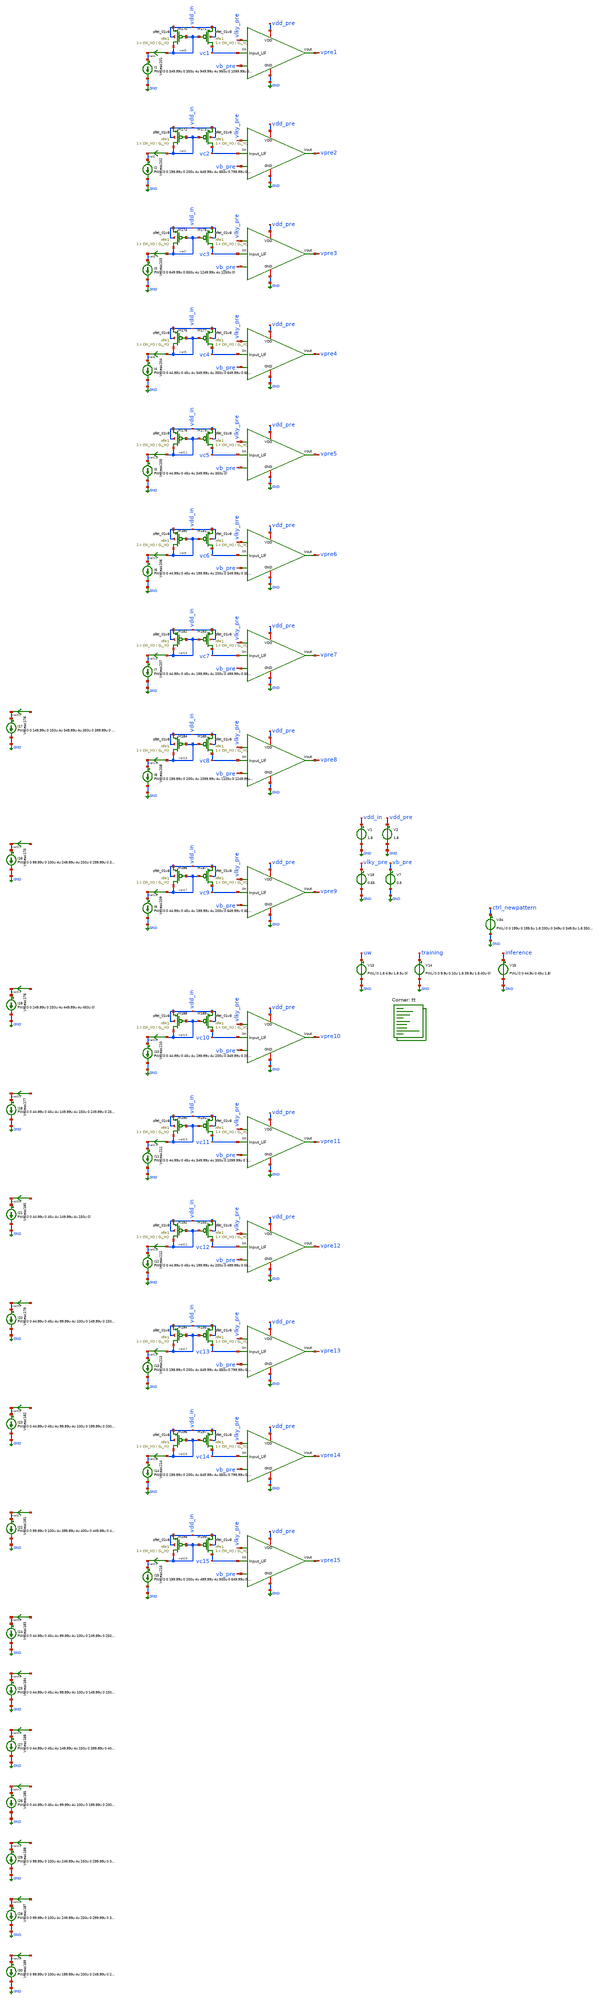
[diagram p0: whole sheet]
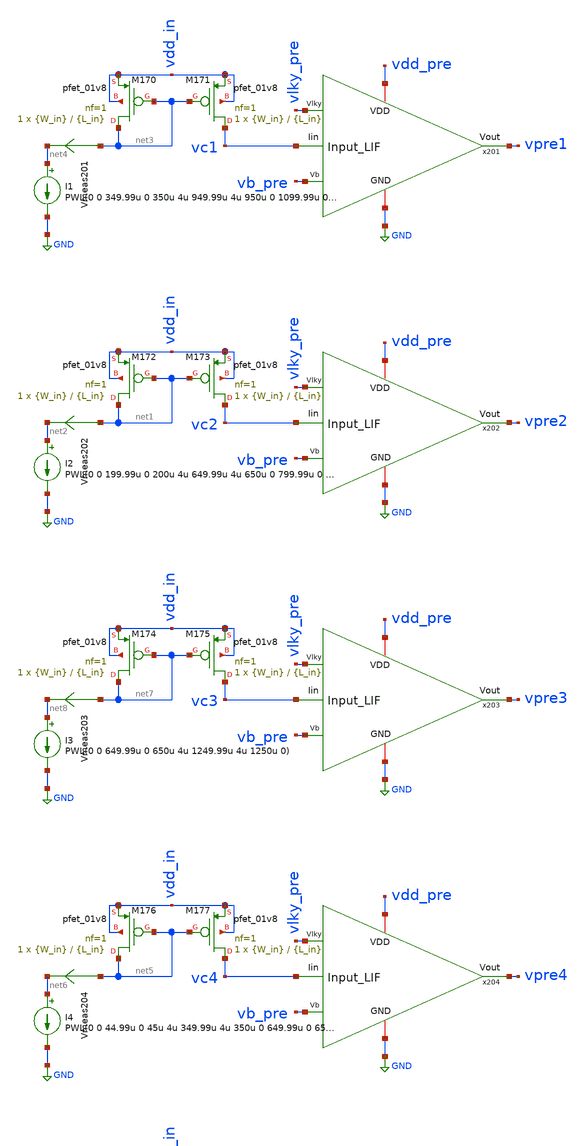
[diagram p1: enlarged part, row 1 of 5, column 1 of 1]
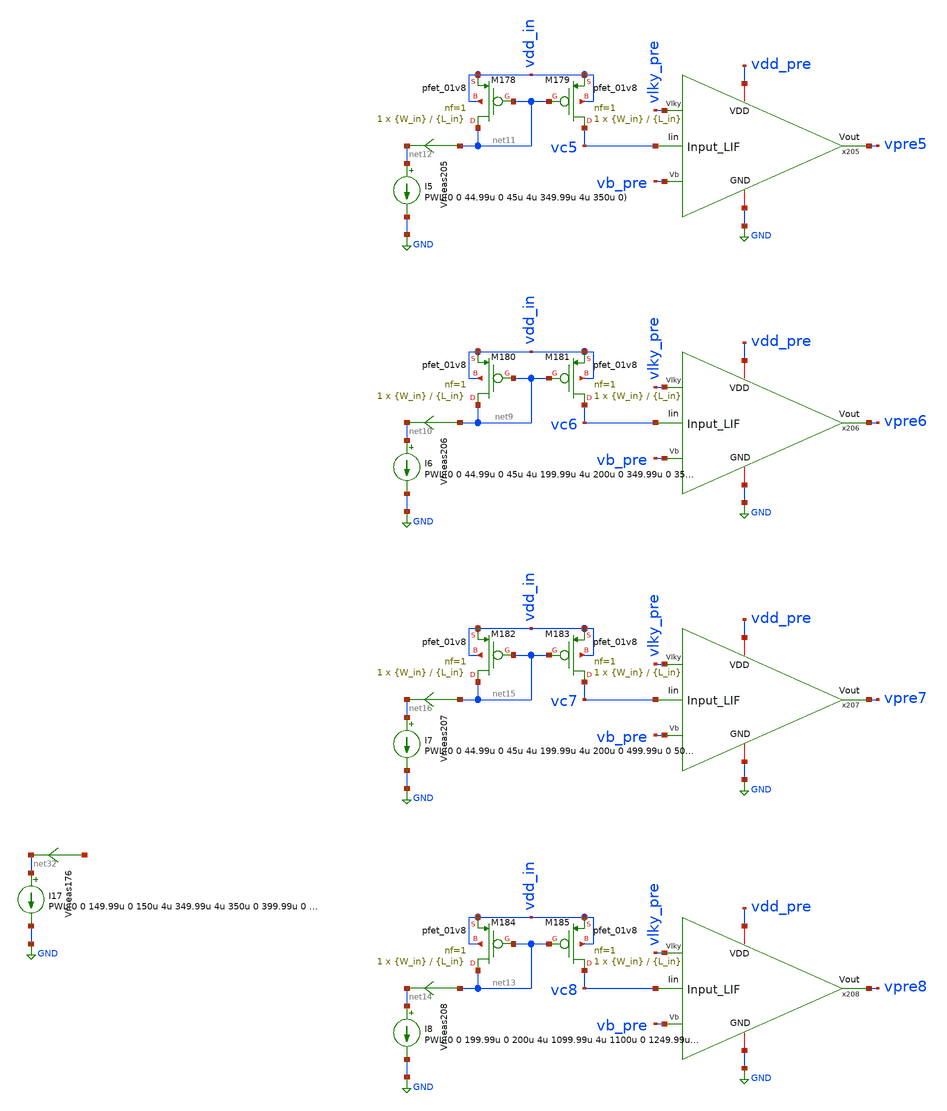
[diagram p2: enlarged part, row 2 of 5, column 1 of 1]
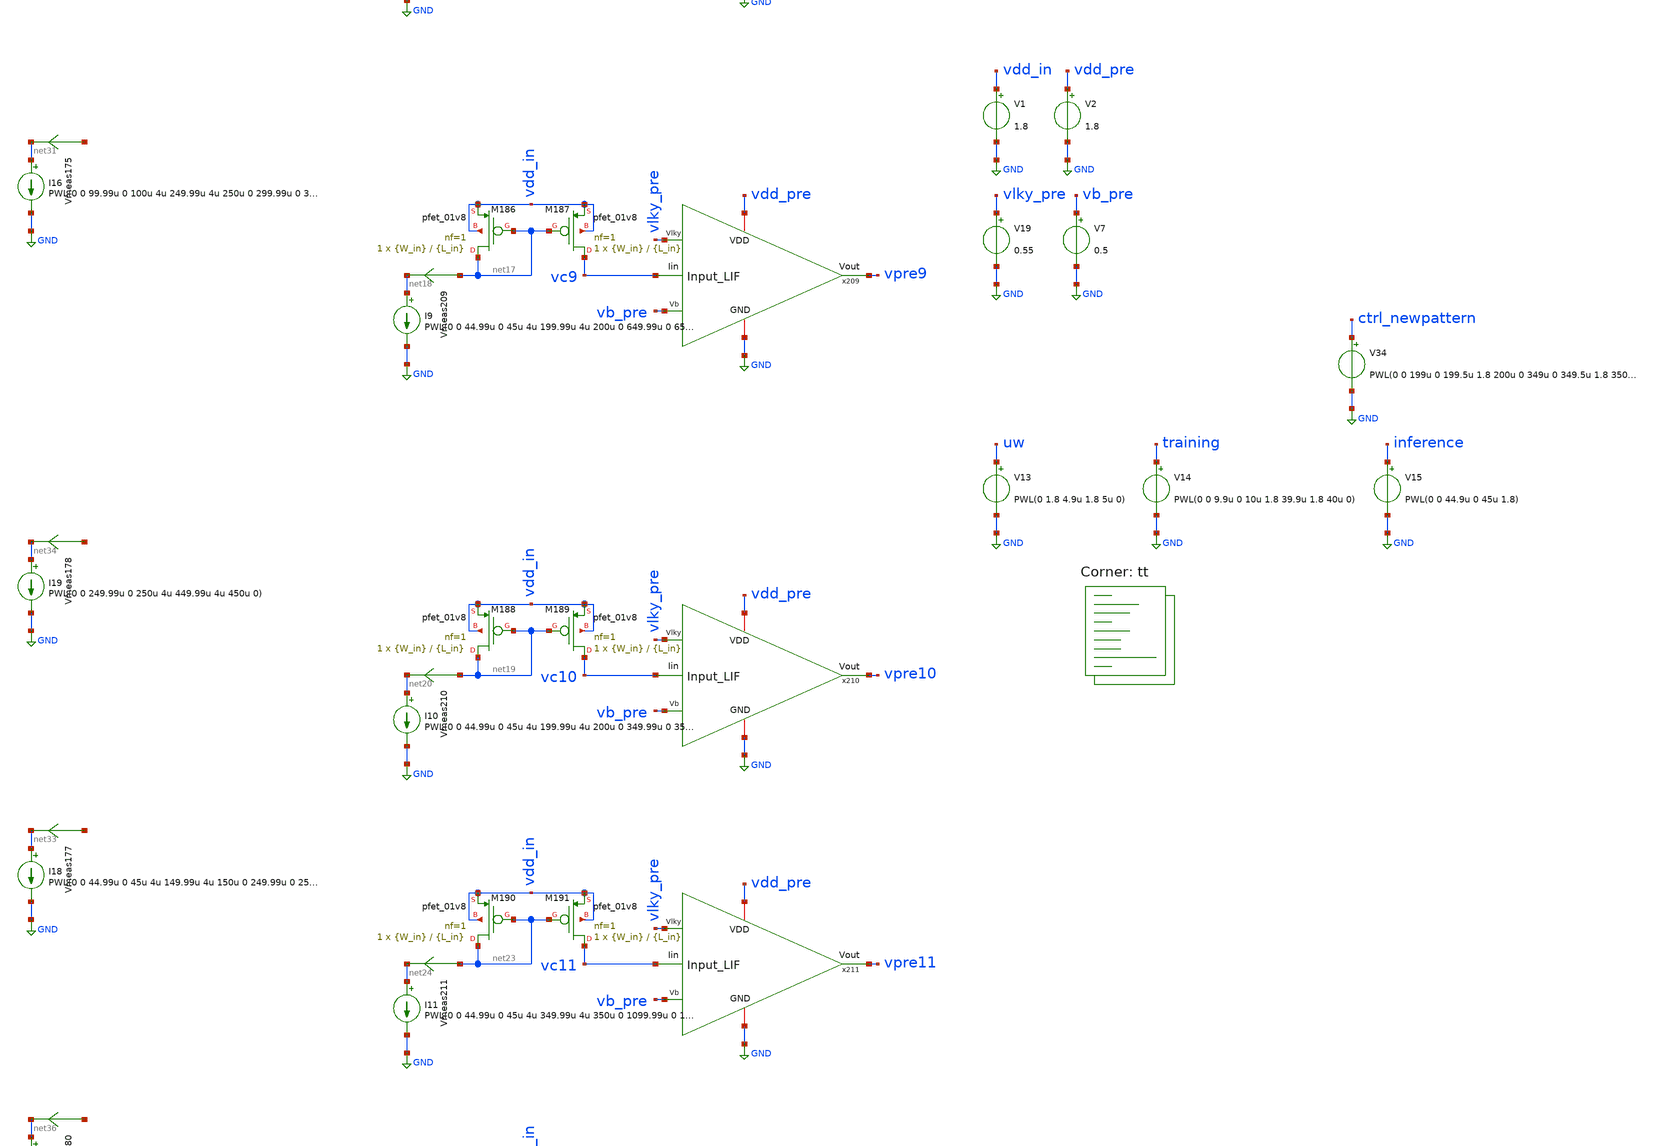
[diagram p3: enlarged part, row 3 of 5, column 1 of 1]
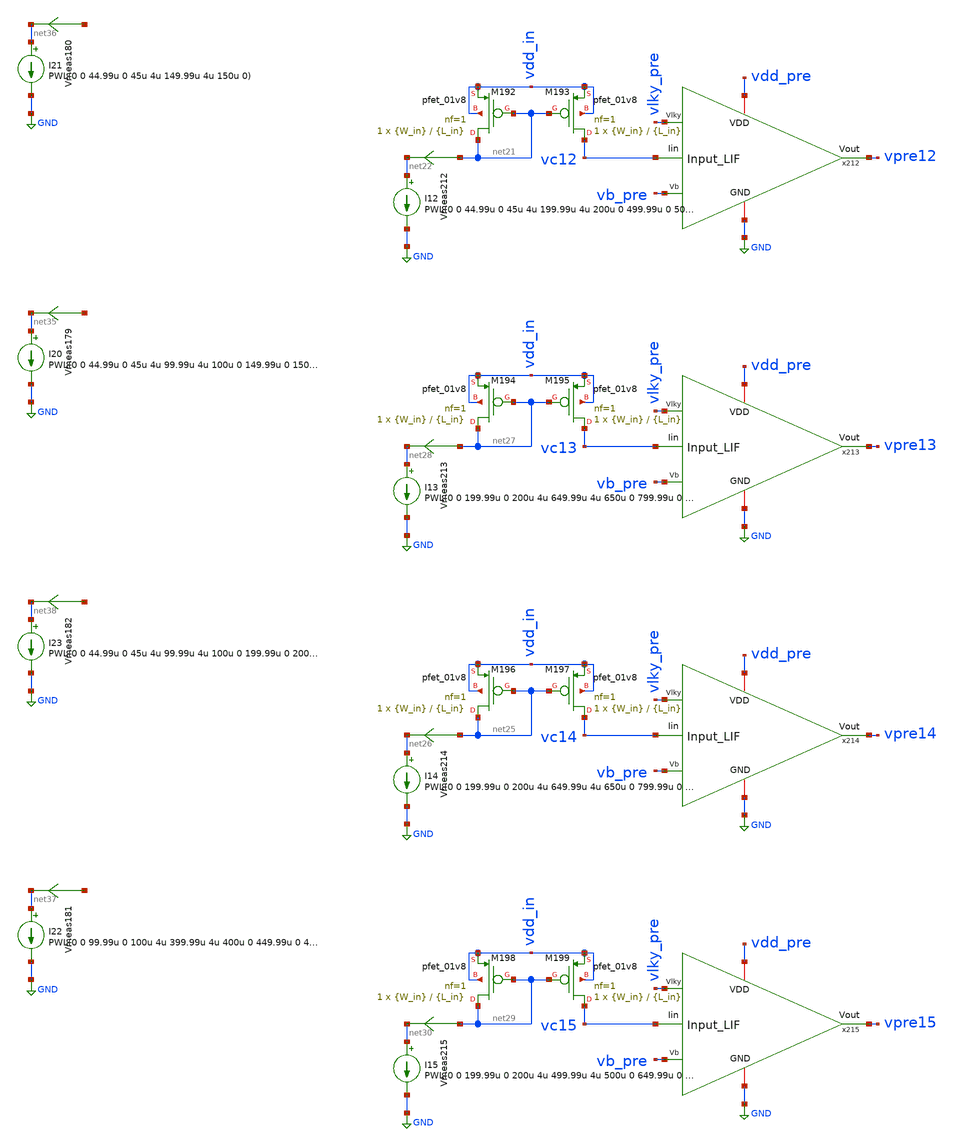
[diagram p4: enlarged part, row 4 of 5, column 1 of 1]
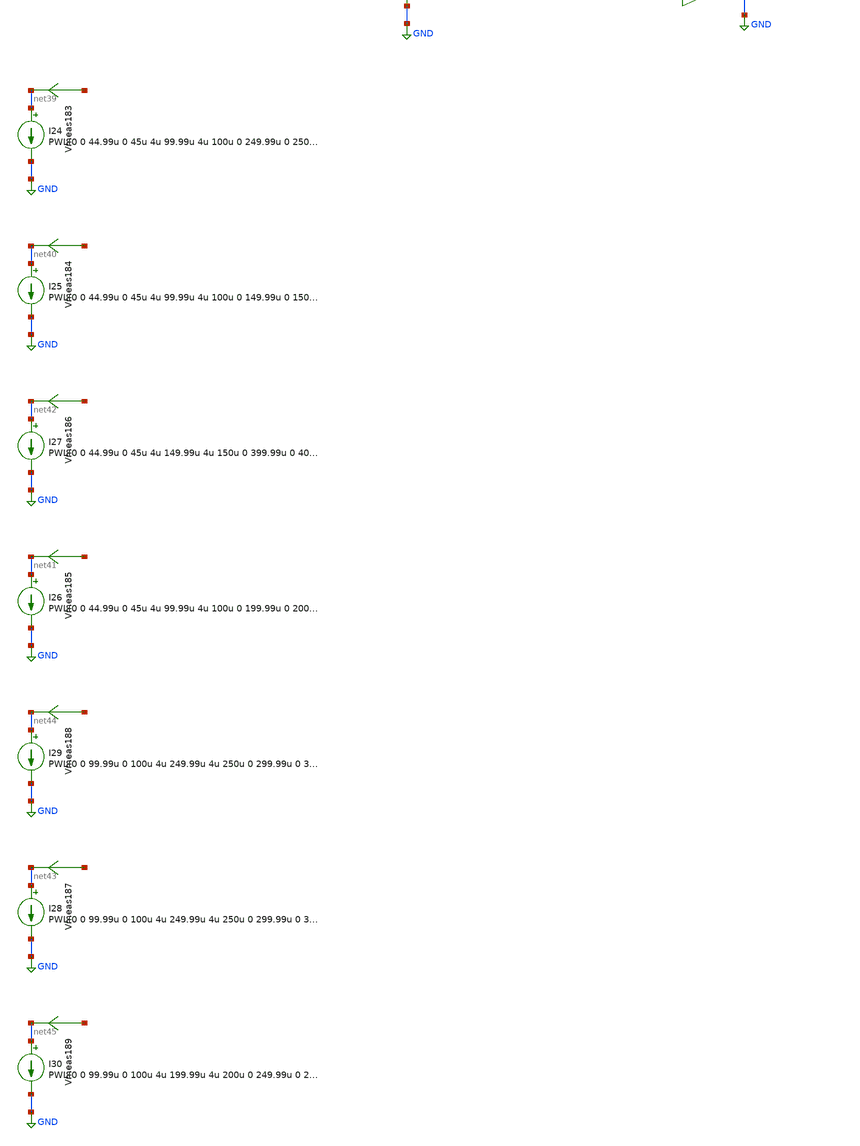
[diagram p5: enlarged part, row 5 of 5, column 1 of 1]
** sch_path: SNN/LIF_15Inputs_tb.sch
**.subckt LIF_15Inputs_tb
V1 vdd_in GND 1.8
V2 vdd_pre GND 1.8
I2 net2 GND PWL(0 0 199.99u 0 200u 4u 649.99u 4u 650u 0 799.99u 0 800u 4u)
XM173 vc2 net1 vdd_in vdd_in sky130_fd_pr__pfet_01v8 L={L_in} W={W_in} nf=1 ad='int((nf+1)/2) * W/nf * 0.29'
+ as='int((nf+2)/2) * W/nf * 0.29' pd='2*int((nf+1)/2) * (W/nf + 0.29)' ps='2*int((nf+2)/2) * (W/nf + 0.29)'
+ nrd='0.29 / W' nrs='0.29 / W' sa=0 sb=0 sd=0 mult=1 m=1
XM172 net1 net1 vdd_in vdd_in sky130_fd_pr__pfet_01v8 L={L_in} W={W_in} nf=1 ad='int((nf+1)/2) * W/nf * 0.29'
+ as='int((nf+2)/2) * W/nf * 0.29' pd='2*int((nf+1)/2) * (W/nf + 0.29)' ps='2*int((nf+2)/2) * (W/nf + 0.29)'
+ nrd='0.29 / W' nrs='0.29 / W' sa=0 sb=0 sd=0 mult=1 m=1
V13 uw GND PWL(0 1.8 4.9u 1.8 5u 0)
V14 training GND PWL(0 0 9.9u 0 10u 1.8 39.9u 1.8 40u 0)
V15 inference GND PWL(0 0 44.9u 0 45u 1.8)
Vmeas202 net1 net2 0
.save i(vmeas202)
V7 vb_pre GND 0.5
I1 net4 GND PWL(0 0 349.99u 0 350u 4u 949.99u 4u 950u 0 1099.99u 0 1100u 4u 1249.99u 4u 1250u 0)
XM171 vc1 net3 vdd_in vdd_in sky130_fd_pr__pfet_01v8 L={L_in} W={W_in} nf=1 ad='int((nf+1)/2) * W/nf * 0.29'
+ as='int((nf+2)/2) * W/nf * 0.29' pd='2*int((nf+1)/2) * (W/nf + 0.29)' ps='2*int((nf+2)/2) * (W/nf + 0.29)'
+ nrd='0.29 / W' nrs='0.29 / W' sa=0 sb=0 sd=0 mult=1 m=1
XM170 net3 net3 vdd_in vdd_in sky130_fd_pr__pfet_01v8 L={L_in} W={W_in} nf=1 ad='int((nf+1)/2) * W/nf * 0.29'
+ as='int((nf+2)/2) * W/nf * 0.29' pd='2*int((nf+1)/2) * (W/nf + 0.29)' ps='2*int((nf+2)/2) * (W/nf + 0.29)'
+ nrd='0.29 / W' nrs='0.29 / W' sa=0 sb=0 sd=0 mult=1 m=1
Vmeas201 net3 net4 0
.save i(vmeas201)
V19 vlky_pre GND 0.55
I4 net6 GND PWL(0 0 44.99u 0 45u 4u 349.99u 4u 350u 0 649.99u 0 650u 4u 1099.99u 4u 1100u 0 1249.99u
+ 0 1250u 4u)
XM177 vc4 net5 vdd_in vdd_in sky130_fd_pr__pfet_01v8 L={L_in} W={W_in} nf=1 ad='int((nf+1)/2) * W/nf * 0.29'
+ as='int((nf+2)/2) * W/nf * 0.29' pd='2*int((nf+1)/2) * (W/nf + 0.29)' ps='2*int((nf+2)/2) * (W/nf + 0.29)'
+ nrd='0.29 / W' nrs='0.29 / W' sa=0 sb=0 sd=0 mult=1 m=1
XM176 net5 net5 vdd_in vdd_in sky130_fd_pr__pfet_01v8 L={L_in} W={W_in} nf=1 ad='int((nf+1)/2) * W/nf * 0.29'
+ as='int((nf+2)/2) * W/nf * 0.29' pd='2*int((nf+1)/2) * (W/nf + 0.29)' ps='2*int((nf+2)/2) * (W/nf + 0.29)'
+ nrd='0.29 / W' nrs='0.29 / W' sa=0 sb=0 sd=0 mult=1 m=1
Vmeas204 net5 net6 0
.save i(vmeas204)
I3 net8 GND PWL(0 0 649.99u 0 650u 4u 1249.99u 4u 1250u 0)
XM175 vc3 net7 vdd_in vdd_in sky130_fd_pr__pfet_01v8 L={L_in} W={W_in} nf=1 ad='int((nf+1)/2) * W/nf * 0.29'
+ as='int((nf+2)/2) * W/nf * 0.29' pd='2*int((nf+1)/2) * (W/nf + 0.29)' ps='2*int((nf+2)/2) * (W/nf + 0.29)'
+ nrd='0.29 / W' nrs='0.29 / W' sa=0 sb=0 sd=0 mult=1 m=1
XM174 net7 net7 vdd_in vdd_in sky130_fd_pr__pfet_01v8 L={L_in} W={W_in} nf=1 ad='int((nf+1)/2) * W/nf * 0.29'
+ as='int((nf+2)/2) * W/nf * 0.29' pd='2*int((nf+1)/2) * (W/nf + 0.29)' ps='2*int((nf+2)/2) * (W/nf + 0.29)'
+ nrd='0.29 / W' nrs='0.29 / W' sa=0 sb=0 sd=0 mult=1 m=1
Vmeas203 net7 net8 0
.save i(vmeas203)
I6 net10 GND PWL(0 0 44.99u 0 45u 4u 199.99u 4u 200u 0 349.99u 0 350u 4u 799.99u 4u 800u 0 1099.99u
+ 0 1100u 4u)
XM181 vc6 net9 vdd_in vdd_in sky130_fd_pr__pfet_01v8 L={L_in} W={W_in} nf=1 ad='int((nf+1)/2) * W/nf * 0.29'
+ as='int((nf+2)/2) * W/nf * 0.29' pd='2*int((nf+1)/2) * (W/nf + 0.29)' ps='2*int((nf+2)/2) * (W/nf + 0.29)'
+ nrd='0.29 / W' nrs='0.29 / W' sa=0 sb=0 sd=0 mult=1 m=1
XM180 net9 net9 vdd_in vdd_in sky130_fd_pr__pfet_01v8 L={L_in} W={W_in} nf=1 ad='int((nf+1)/2) * W/nf * 0.29'
+ as='int((nf+2)/2) * W/nf * 0.29' pd='2*int((nf+1)/2) * (W/nf + 0.29)' ps='2*int((nf+2)/2) * (W/nf + 0.29)'
+ nrd='0.29 / W' nrs='0.29 / W' sa=0 sb=0 sd=0 mult=1 m=1
Vmeas206 net9 net10 0
.save i(vmeas206)
I5 net12 GND PWL(0 0 44.99u 0 45u 4u 349.99u 4u 350u 0)
XM179 vc5 net11 vdd_in vdd_in sky130_fd_pr__pfet_01v8 L={L_in} W={W_in} nf=1 ad='int((nf+1)/2) * W/nf * 0.29'
+ as='int((nf+2)/2) * W/nf * 0.29' pd='2*int((nf+1)/2) * (W/nf + 0.29)' ps='2*int((nf+2)/2) * (W/nf + 0.29)'
+ nrd='0.29 / W' nrs='0.29 / W' sa=0 sb=0 sd=0 mult=1 m=1
XM178 net11 net11 vdd_in vdd_in sky130_fd_pr__pfet_01v8 L={L_in} W={W_in} nf=1 ad='int((nf+1)/2) * W/nf * 0.29'
+ as='int((nf+2)/2) * W/nf * 0.29' pd='2*int((nf+1)/2) * (W/nf + 0.29)' ps='2*int((nf+2)/2) * (W/nf + 0.29)'
+ nrd='0.29 / W' nrs='0.29 / W' sa=0 sb=0 sd=0 mult=1 m=1
Vmeas205 net11 net12 0
.save i(vmeas205)
I8 net14 GND PWL(0 0 199.99u 0 200u 4u 1099.99u 4u 1100u 0 1249.99u 0 1250u 4u)
XM185 vc8 net13 vdd_in vdd_in sky130_fd_pr__pfet_01v8 L={L_in} W={W_in} nf=1 ad='int((nf+1)/2) * W/nf * 0.29'
+ as='int((nf+2)/2) * W/nf * 0.29' pd='2*int((nf+1)/2) * (W/nf + 0.29)' ps='2*int((nf+2)/2) * (W/nf + 0.29)'
+ nrd='0.29 / W' nrs='0.29 / W' sa=0 sb=0 sd=0 mult=1 m=1
XM184 net13 net13 vdd_in vdd_in sky130_fd_pr__pfet_01v8 L={L_in} W={W_in} nf=1 ad='int((nf+1)/2) * W/nf * 0.29'
+ as='int((nf+2)/2) * W/nf * 0.29' pd='2*int((nf+1)/2) * (W/nf + 0.29)' ps='2*int((nf+2)/2) * (W/nf + 0.29)'
+ nrd='0.29 / W' nrs='0.29 / W' sa=0 sb=0 sd=0 mult=1 m=1
Vmeas208 net13 net14 0
.save i(vmeas208)
I7 net16 GND PWL(0 0 44.99u 0 45u 4u 199.99u 4u 200u 0 499.99u 0 500u 4u 649.99u 4u 650u 0 949.99u 0
+ 950u 4u 1099.99u 4u 1100u 0)
XM183 vc7 net15 vdd_in vdd_in sky130_fd_pr__pfet_01v8 L={L_in} W={W_in} nf=1 ad='int((nf+1)/2) * W/nf * 0.29'
+ as='int((nf+2)/2) * W/nf * 0.29' pd='2*int((nf+1)/2) * (W/nf + 0.29)' ps='2*int((nf+2)/2) * (W/nf + 0.29)'
+ nrd='0.29 / W' nrs='0.29 / W' sa=0 sb=0 sd=0 mult=1 m=1
XM182 net15 net15 vdd_in vdd_in sky130_fd_pr__pfet_01v8 L={L_in} W={W_in} nf=1 ad='int((nf+1)/2) * W/nf * 0.29'
+ as='int((nf+2)/2) * W/nf * 0.29' pd='2*int((nf+1)/2) * (W/nf + 0.29)' ps='2*int((nf+2)/2) * (W/nf + 0.29)'
+ nrd='0.29 / W' nrs='0.29 / W' sa=0 sb=0 sd=0 mult=1 m=1
Vmeas207 net15 net16 0
.save i(vmeas207)
I9 net18 GND PWL(0 0 44.99u 0 45u 4u 199.99u 4u 200u 0 649.99u 0 650u 4u 799.99u 4u 800u 0 1099.99u
+ 0 1100u 4u 1249.99u 4u 1250u 0 1399.99u 0 1400u 4u)
XM187 vc9 net17 vdd_in vdd_in sky130_fd_pr__pfet_01v8 L={L_in} W={W_in} nf=1 ad='int((nf+1)/2) * W/nf * 0.29'
+ as='int((nf+2)/2) * W/nf * 0.29' pd='2*int((nf+1)/2) * (W/nf + 0.29)' ps='2*int((nf+2)/2) * (W/nf + 0.29)'
+ nrd='0.29 / W' nrs='0.29 / W' sa=0 sb=0 sd=0 mult=1 m=1
XM186 net17 net17 vdd_in vdd_in sky130_fd_pr__pfet_01v8 L={L_in} W={W_in} nf=1 ad='int((nf+1)/2) * W/nf * 0.29'
+ as='int((nf+2)/2) * W/nf * 0.29' pd='2*int((nf+1)/2) * (W/nf + 0.29)' ps='2*int((nf+2)/2) * (W/nf + 0.29)'
+ nrd='0.29 / W' nrs='0.29 / W' sa=0 sb=0 sd=0 mult=1 m=1
Vmeas209 net17 net18 0
.save i(vmeas209)
I10 net20 GND PWL(0 0 44.99u 0 45u 4u 199.99u 4u 200u 0 349.99u 0 350u 4u 499.99u 4u 500u 0 949.99u
+ 0 950u 4u 1099.99u 4u 1100u 0 1249.99u 0 1250u 4u 1399.99u 4u 1400u 0)
XM189 vc10 net19 vdd_in vdd_in sky130_fd_pr__pfet_01v8 L={L_in} W={W_in} nf=1 ad='int((nf+1)/2) * W/nf * 0.29'
+ as='int((nf+2)/2) * W/nf * 0.29' pd='2*int((nf+1)/2) * (W/nf + 0.29)' ps='2*int((nf+2)/2) * (W/nf + 0.29)'
+ nrd='0.29 / W' nrs='0.29 / W' sa=0 sb=0 sd=0 mult=1 m=1
XM188 net19 net19 vdd_in vdd_in sky130_fd_pr__pfet_01v8 L={L_in} W={W_in} nf=1 ad='int((nf+1)/2) * W/nf * 0.29'
+ as='int((nf+2)/2) * W/nf * 0.29' pd='2*int((nf+1)/2) * (W/nf + 0.29)' ps='2*int((nf+2)/2) * (W/nf + 0.29)'
+ nrd='0.29 / W' nrs='0.29 / W' sa=0 sb=0 sd=0 mult=1 m=1
Vmeas210 net19 net20 0
.save i(vmeas210)
I12 net22 GND PWL(0 0 44.99u 0 45u 4u 199.99u 4u 200u 0 499.99u 0 500u 4u 1099.99u 4u 1100u 0
+ 1249.99u 0 1250u 4u)
XM193 vc12 net21 vdd_in vdd_in sky130_fd_pr__pfet_01v8 L={L_in} W={W_in} nf=1 ad='int((nf+1)/2) * W/nf * 0.29'
+ as='int((nf+2)/2) * W/nf * 0.29' pd='2*int((nf+1)/2) * (W/nf + 0.29)' ps='2*int((nf+2)/2) * (W/nf + 0.29)'
+ nrd='0.29 / W' nrs='0.29 / W' sa=0 sb=0 sd=0 mult=1 m=1
XM192 net21 net21 vdd_in vdd_in sky130_fd_pr__pfet_01v8 L={L_in} W={W_in} nf=1 ad='int((nf+1)/2) * W/nf * 0.29'
+ as='int((nf+2)/2) * W/nf * 0.29' pd='2*int((nf+1)/2) * (W/nf + 0.29)' ps='2*int((nf+2)/2) * (W/nf + 0.29)'
+ nrd='0.29 / W' nrs='0.29 / W' sa=0 sb=0 sd=0 mult=1 m=1
Vmeas212 net21 net22 0
.save i(vmeas212)
I11 net24 GND PWL(0 0 44.99u 0 45u 4u 349.99u 4u 350u 0 1099.99u 0 1100u 4u 1249.99u 4u 1250u 0)
XM191 vc11 net23 vdd_in vdd_in sky130_fd_pr__pfet_01v8 L={L_in} W={W_in} nf=1 ad='int((nf+1)/2) * W/nf * 0.29'
+ as='int((nf+2)/2) * W/nf * 0.29' pd='2*int((nf+1)/2) * (W/nf + 0.29)' ps='2*int((nf+2)/2) * (W/nf + 0.29)'
+ nrd='0.29 / W' nrs='0.29 / W' sa=0 sb=0 sd=0 mult=1 m=1
XM190 net23 net23 vdd_in vdd_in sky130_fd_pr__pfet_01v8 L={L_in} W={W_in} nf=1 ad='int((nf+1)/2) * W/nf * 0.29'
+ as='int((nf+2)/2) * W/nf * 0.29' pd='2*int((nf+1)/2) * (W/nf + 0.29)' ps='2*int((nf+2)/2) * (W/nf + 0.29)'
+ nrd='0.29 / W' nrs='0.29 / W' sa=0 sb=0 sd=0 mult=1 m=1
Vmeas211 net23 net24 0
.save i(vmeas211)
I14 net26 GND PWL(0 0 199.99u 0 200u 4u 649.99u 4u 650u 0 799.99u 0 800u 4u 1099.99u 4u 1100u 0
+ 1249.99u 0 1250u 4u)
XM197 vc14 net25 vdd_in vdd_in sky130_fd_pr__pfet_01v8 L={L_in} W={W_in} nf=1 ad='int((nf+1)/2) * W/nf * 0.29'
+ as='int((nf+2)/2) * W/nf * 0.29' pd='2*int((nf+1)/2) * (W/nf + 0.29)' ps='2*int((nf+2)/2) * (W/nf + 0.29)'
+ nrd='0.29 / W' nrs='0.29 / W' sa=0 sb=0 sd=0 mult=1 m=1
XM196 net25 net25 vdd_in vdd_in sky130_fd_pr__pfet_01v8 L={L_in} W={W_in} nf=1 ad='int((nf+1)/2) * W/nf * 0.29'
+ as='int((nf+2)/2) * W/nf * 0.29' pd='2*int((nf+1)/2) * (W/nf + 0.29)' ps='2*int((nf+2)/2) * (W/nf + 0.29)'
+ nrd='0.29 / W' nrs='0.29 / W' sa=0 sb=0 sd=0 mult=1 m=1
Vmeas214 net25 net26 0
.save i(vmeas214)
I13 net28 GND PWL(0 0 199.99u 0 200u 4u 649.99u 4u 650u 0 799.99u 0 800u 4u 949.99u 4u 950u 0
+ 1099.99u 0 1100u 4u 1249.99u 4u 1250u 0 1399.99u 0 1400u 4u)
XM195 vc13 net27 vdd_in vdd_in sky130_fd_pr__pfet_01v8 L={L_in} W={W_in} nf=1 ad='int((nf+1)/2) * W/nf * 0.29'
+ as='int((nf+2)/2) * W/nf * 0.29' pd='2*int((nf+1)/2) * (W/nf + 0.29)' ps='2*int((nf+2)/2) * (W/nf + 0.29)'
+ nrd='0.29 / W' nrs='0.29 / W' sa=0 sb=0 sd=0 mult=1 m=1
XM194 net27 net27 vdd_in vdd_in sky130_fd_pr__pfet_01v8 L={L_in} W={W_in} nf=1 ad='int((nf+1)/2) * W/nf * 0.29'
+ as='int((nf+2)/2) * W/nf * 0.29' pd='2*int((nf+1)/2) * (W/nf + 0.29)' ps='2*int((nf+2)/2) * (W/nf + 0.29)'
+ nrd='0.29 / W' nrs='0.29 / W' sa=0 sb=0 sd=0 mult=1 m=1
Vmeas213 net27 net28 0
.save i(vmeas213)
I15 net30 GND PWL(0 0 199.99u 0 200u 4u 499.99u 4u 500u 0 649.99u 0 650u 4u 799.99u 4u 800u 0)
XM199 vc15 net29 vdd_in vdd_in sky130_fd_pr__pfet_01v8 L={L_in} W={W_in} nf=1 ad='int((nf+1)/2) * W/nf * 0.29'
+ as='int((nf+2)/2) * W/nf * 0.29' pd='2*int((nf+1)/2) * (W/nf + 0.29)' ps='2*int((nf+2)/2) * (W/nf + 0.29)'
+ nrd='0.29 / W' nrs='0.29 / W' sa=0 sb=0 sd=0 mult=1 m=1
XM198 net29 net29 vdd_in vdd_in sky130_fd_pr__pfet_01v8 L={L_in} W={W_in} nf=1 ad='int((nf+1)/2) * W/nf * 0.29'
+ as='int((nf+2)/2) * W/nf * 0.29' pd='2*int((nf+1)/2) * (W/nf + 0.29)' ps='2*int((nf+2)/2) * (W/nf + 0.29)'
+ nrd='0.29 / W' nrs='0.29 / W' sa=0 sb=0 sd=0 mult=1 m=1
Vmeas215 net29 net30 0
.save i(vmeas215)
V34 ctrl_newpattern GND PWL(0 0 199u 0 199.5u 1.8 200u 0 349u 0 349.5u 1.8 350u 0 499u 0 499.5u 1.8
+ 500u 0 649u 0 649.5u 1.8 650u 0 799u 0 799.5u 1.8 800u 0 949u 0 949.5u 1.8 950u 0 1099u 0 1099.5u 1.8
+ 1100u 0 1249u 0 1249.5u 1.8 1250u 0 1399u 0 1399.5u 1.8 1400u 0)
x201 vlky_pre vb_pre vdd_pre vpre1 GND vc1 Input_LIF
x202 vlky_pre vb_pre vdd_pre vpre2 GND vc2 Input_LIF
x203 vlky_pre vb_pre vdd_pre vpre3 GND vc3 Input_LIF
x204 vlky_pre vb_pre vdd_pre vpre4 GND vc4 Input_LIF
x205 vlky_pre vb_pre vdd_pre vpre5 GND vc5 Input_LIF
x206 vlky_pre vb_pre vdd_pre vpre6 GND vc6 Input_LIF
x207 vlky_pre vb_pre vdd_pre vpre7 GND vc7 Input_LIF
x208 vlky_pre vb_pre vdd_pre vpre8 GND vc8 Input_LIF
x209 vlky_pre vb_pre vdd_pre vpre9 GND vc9 Input_LIF
x210 vlky_pre vb_pre vdd_pre vpre10 GND vc10 Input_LIF
x211 vlky_pre vb_pre vdd_pre vpre11 GND vc11 Input_LIF
x212 vlky_pre vb_pre vdd_pre vpre12 GND vc12 Input_LIF
x213 vlky_pre vb_pre vdd_pre vpre13 GND vc13 Input_LIF
x214 vlky_pre vb_pre vdd_pre vpre14 GND vc14 Input_LIF
x215 vlky_pre vb_pre vdd_pre vpre15 GND vc15 Input_LIF
I16 net31 GND PWL(0 0 99.99u 0 100u 4u 249.99u 4u 250u 0 299.99u 0 300u 4u)
Vmeas175 net46 net31 0
.save i(vmeas175)
I17 net32 GND PWL(0 0 149.99u 0 150u 4u 349.99u 4u 350u 0 399.99u 0 400u 4u 449.99u 4u 450u 0)
Vmeas176 net47 net32 0
.save i(vmeas176)
I18 net33 GND PWL(0 0 44.99u 0 45u 4u 149.99u 4u 150u 0 249.99u 0 250u 4u 399.99u 4u 400u 0 449.99u
+ 0 450u 4u)
Vmeas177 net48 net33 0
.save i(vmeas177)
I19 net34 GND PWL(0 0 249.99u 0 250u 4u 449.99u 4u 450u 0)
Vmeas178 net49 net34 0
.save i(vmeas178)
I20 net35 GND PWL(0 0 44.99u 0 45u 4u 99.99u 4u 100u 0 149.99u 0 150u 4u 299.99u 4u 300u 0 399.99u 0
+ 400u 4u)
Vmeas179 net50 net35 0
.save i(vmeas179)
I21 net36 GND PWL(0 0 44.99u 0 45u 4u 149.99u 4u 150u 0)
Vmeas180 net51 net36 0
.save i(vmeas180)
I22 net37 GND PWL(0 0 99.99u 0 100u 4u 399.99u 4u 400u 0 449.99u 0 450u 4u)
Vmeas181 net52 net37 0
.save i(vmeas181)
I23 net38 GND PWL(0 0 44.99u 0 45u 4u 99.99u 4u 100u 0 199.99u 0 200u 4u 249.99u 4u 250u 0 349.99u 0
+ 350u 4u 399.99u 4u 400u 0)
Vmeas182 net53 net38 0
.save i(vmeas182)
I24 net39 GND PWL(0 0 44.99u 0 45u 4u 99.99u 4u 100u 0 249.99u 0 250u 4u 299.99u 4u 300u 0 399.99u 0
+ 400u 4u 449.99u 4u 450u 0 499.99u 0 500u 4u)
Vmeas183 net54 net39 0
.save i(vmeas183)
I25 net40 GND PWL(0 0 44.99u 0 45u 4u 99.99u 4u 100u 0 149.99u 0 150u 4u 199.99u 4u 200u 0 349.99u 0
+ 350u 4u 399.99u 4u 400u 0 449.99u 0 450u 4u 499.99u 4u 500u 0)
Vmeas184 net55 net40 0
.save i(vmeas184)
I26 net41 GND PWL(0 0 44.99u 0 45u 4u 99.99u 4u 100u 0 199.99u 0 200u 4u 399.99u 4u 400u 0 449.99u 0
+ 450u 4u)
Vmeas185 net56 net41 0
.save i(vmeas185)
I27 net42 GND PWL(0 0 44.99u 0 45u 4u 149.99u 4u 150u 0 399.99u 0 400u 4u 449.99u 4u 450u 0)
Vmeas186 net57 net42 0
.save i(vmeas186)
I28 net43 GND PWL(0 0 99.99u 0 100u 4u 249.99u 4u 250u 0 299.99u 0 300u 4u 399.99u 4u 400u 0 449.99u
+ 0 450u 4u 499.99u 4u 500u 0)
Vmeas187 net58 net43 0
.save i(vmeas187)
I29 net44 GND PWL(0 0 99.99u 0 100u 4u 249.99u 4u 250u 0 299.99u 0 300u 4u 349.99u 4u 350u 0 399.99u
+ 0 400u 4u 449.99u 4u 450u 0)
Vmeas188 net59 net44 0
.save i(vmeas188)
I30 net45 GND PWL(0 0 99.99u 0 100u 4u 199.99u 4u 200u 0 249.99u 0 250u 4u 299.99u 4u 300u 0 499.99u
+ 0 500u 4u)
Vmeas189 net60 net45 0
.save i(vmeas189)
**** begin user architecture code
.lib $::SKYWATER_MODELS/sky130.lib.spice tt

** opencircuitdesign pdks install
.inc $::SKYWATER_MODELS/rram_v0.spice



.option set_threads = 16
.option klu
*--Current Injection--*
.param L_in=0.15
.param W_in=1
.control
	save all
	tran 100n 1550u 0
	write LIF_15Inputs_tb.raw v(vpre1) v(vpre2) v(vpre3) v(vpre4) v(vpre5) v(vpre6) v(vpre7) v(vpre8)
+ v(vpre9) v(vpre10) v(vpre11) v(vpre12) v(vpre13) v(vpre14) v(vpre15) v(ctrl_newpattern)
	*wrdata SNN_15x1_lt_tb.ssv v(8)
.endc


**** end user architecture code
**.ends

* expanding   symbol:  /home/ricardo/RATT_repos/Proyectos_xschem/SNN/Input_LIF.sym # of pins=6
** sym_path: Final_Design/Input_LIF.sym
** sch_path: Final_Design/Input_LIF.sch
.subckt Input_LIF Vlky Vb VDD Vout GND Iin
*.iopin GND
*.ipin Vb
*.iopin VDD
*.opin Vout
*.ipin Iin
*.ipin Vlky
XM5 net3 Vb GND GND sky130_fd_pr__nfet_01v8 L=0.15 W=5 nf=1 ad='int((nf+1)/2) * W/nf * 0.29' as='int((nf+2)/2) * W/nf * 0.29'
+ pd='2*int((nf+1)/2) * (W/nf + 0.29)' ps='2*int((nf+2)/2) * (W/nf + 0.29)' nrd='0.29 / W' nrs='0.29 / W'
+ sa=0 sb=0 sd=0 mult=1 m=1
XM4 net1 net2 net3 GND sky130_fd_pr__nfet_01v8 L=0.15 W=1.5 nf=1 ad='int((nf+1)/2) * W/nf * 0.29' as='int((nf+2)/2) * W/nf * 0.29'
+ pd='2*int((nf+1)/2) * (W/nf + 0.29)' ps='2*int((nf+2)/2) * (W/nf + 0.29)' nrd='0.29 / W' nrs='0.29 / W'
+ sa=0 sb=0 sd=0 mult=1 m=1
XM3 net1 net2 VDD VDD sky130_fd_pr__pfet_01v8 L=20 W=1 nf=1 ad='int((nf+1)/2) * W/nf * 0.29' as='int((nf+2)/2) * W/nf * 0.29'
+ pd='2*int((nf+1)/2) * (W/nf + 0.29)' ps='2*int((nf+2)/2) * (W/nf + 0.29)' nrd='0.29 / W' nrs='0.29 / W'
+ sa=0 sb=0 sd=0 mult=1 m=1
XC2 net1 GND sky130_fd_pr__cap_mim_m3_1 W=10 L=5 MF=1 m=1
XM2 Iin net1 GND GND sky130_fd_pr__nfet_01v8 L=20 W=1 nf=1 ad='int((nf+1)/2) * W/nf * 0.29' as='int((nf+2)/2) * W/nf * 0.29'
+ pd='2*int((nf+1)/2) * (W/nf + 0.29)' ps='2*int((nf+2)/2) * (W/nf + 0.29)' nrd='0.29 / W' nrs='0.29 / W'
+ sa=0 sb=0 sd=0 mult=1 m=1
XC1 Iin GND sky130_fd_pr__cap_mim_m3_1 W=20 L=20 MF=1 m=1
XM10 net4 Vout GND GND sky130_fd_pr__nfet_01v8 L=0.15 W=1.5 nf=1 ad='int((nf+1)/2) * W/nf * 0.29' as='int((nf+2)/2) * W/nf * 0.29'
+ pd='2*int((nf+1)/2) * (W/nf + 0.29)' ps='2*int((nf+2)/2) * (W/nf + 0.29)' nrd='0.29 / W' nrs='0.29 / W'
+ sa=0 sb=0 sd=0 mult=1 m=1
XM7 net2 Iin net4 GND sky130_fd_pr__nfet_01v8 L=0.15 W=1.5 nf=1 ad='int((nf+1)/2) * W/nf * 0.29' as='int((nf+2)/2) * W/nf * 0.29'
+ pd='2*int((nf+1)/2) * (W/nf + 0.29)' ps='2*int((nf+2)/2) * (W/nf + 0.29)' nrd='0.29 / W' nrs='0.29 / W'
+ sa=0 sb=0 sd=0 mult=1 m=1
XM6 net2 Iin VDD VDD sky130_fd_pr__pfet_01v8 L=0.15 W=1.5 nf=1 ad='int((nf+1)/2) * W/nf * 0.29' as='int((nf+2)/2) * W/nf * 0.29'
+ pd='2*int((nf+1)/2) * (W/nf + 0.29)' ps='2*int((nf+2)/2) * (W/nf + 0.29)' nrd='0.29 / W' nrs='0.29 / W'
+ sa=0 sb=0 sd=0 mult=1 m=1
XM9 Vout net2 net4 GND sky130_fd_pr__nfet_01v8 L=0.15 W=1.5 nf=1 ad='int((nf+1)/2) * W/nf * 0.29' as='int((nf+2)/2) * W/nf * 0.29'
+ pd='2*int((nf+1)/2) * (W/nf + 0.29)' ps='2*int((nf+2)/2) * (W/nf + 0.29)' nrd='0.29 / W' nrs='0.29 / W'
+ sa=0 sb=0 sd=0 mult=1 m=1
XM8 Vout net2 VDD VDD sky130_fd_pr__pfet_01v8 L=0.15 W=5 nf=1 ad='int((nf+1)/2) * W/nf * 0.29' as='int((nf+2)/2) * W/nf * 0.29'
+ pd='2*int((nf+1)/2) * (W/nf + 0.29)' ps='2*int((nf+2)/2) * (W/nf + 0.29)' nrd='0.29 / W' nrs='0.29 / W'
+ sa=0 sb=0 sd=0 mult=1 m=1
XM1 Iin Vlky GND GND sky130_fd_pr__nfet_01v8 L=0.15 W=1.5 nf=1 ad='int((nf+1)/2) * W/nf * 0.29' as='int((nf+2)/2) * W/nf * 0.29'
+ pd='2*int((nf+1)/2) * (W/nf + 0.29)' ps='2*int((nf+2)/2) * (W/nf + 0.29)' nrd='0.29 / W' nrs='0.29 / W'
+ sa=0 sb=0 sd=0 mult=1 m=1
.ends

.GLOBAL GND
.end
